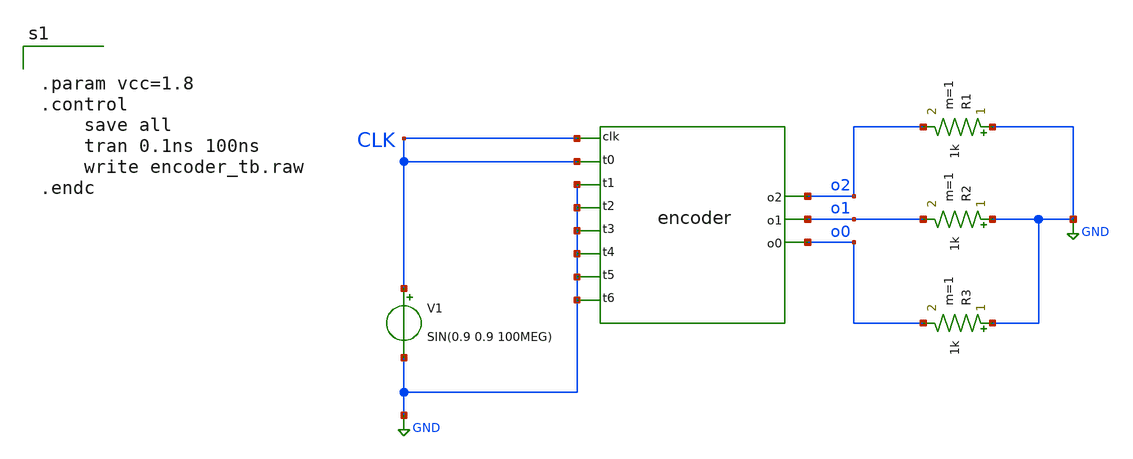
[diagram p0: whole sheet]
** sch_path: tt_um_emmersonv_tiq_adc/xschem/encoder_tb.sch
**.subckt encoder_tb
V1 CLK GND SIN(0.9 0.9 100MEG)
ADUT [ CLK CLK GND GND GND GND GND GND ] [ o0 o1 o2 ] dut
R1 GND o2 1k m=1
R2 GND o1 1k m=1
R3 GND o0 1k m=1
**** begin user architecture code


.param vcc=1.8
.control
	save all
	tran 0.1ns 100ns
	write encoder_tb.raw
.endc


**** end user architecture code
**.ends
.GLOBAL GND
**** begin user architecture code
.model dut d_cosim simulation="./encoder.so"
**** end user architecture code
.end
